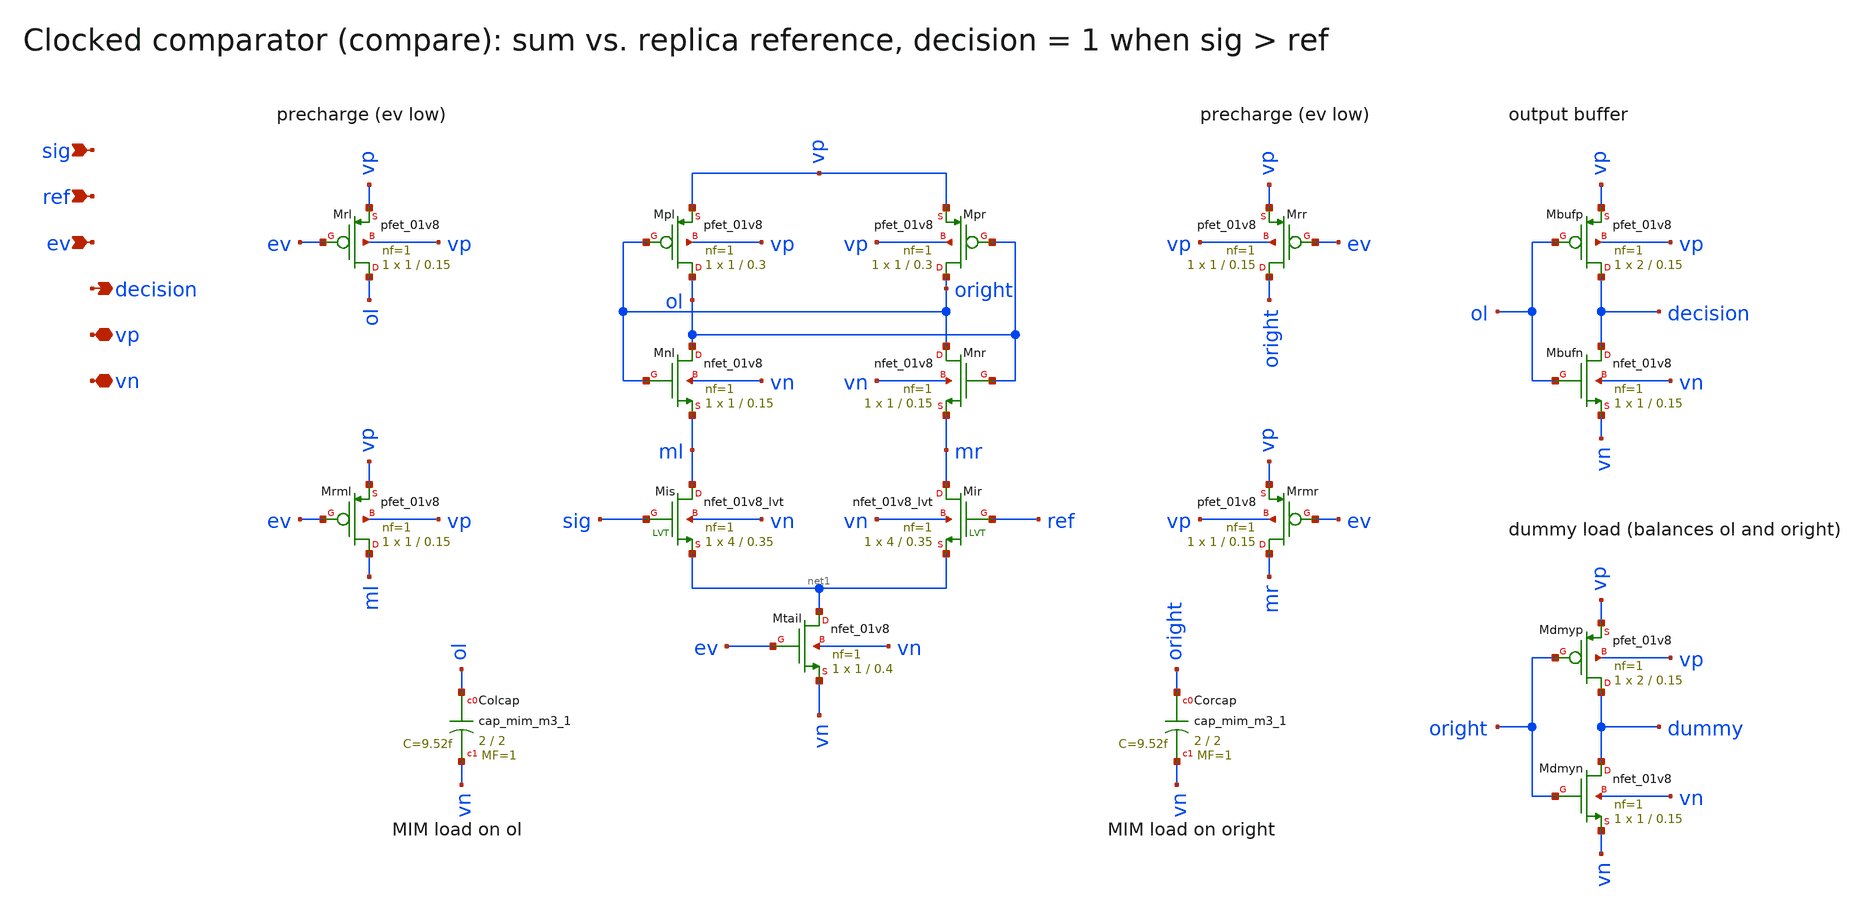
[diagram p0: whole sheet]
** sch_path: xschem/compare.sch
**.subckt compare sig ref ev decision vp vn
*.ipin sig
*.ipin ref
*.ipin ev
*.opin decision
*.iopin vp
*.iopin vn
XMpl ol oright vp vp sky130_fd_pr__pfet_01v8 L=0.3 W=1 nf=1 ad='int((nf+1)/2) * W/nf * 0.29' as='int((nf+2)/2) * W/nf * 0.29'
+ pd='2*int((nf+1)/2) * (W/nf + 0.29)' ps='2*int((nf+2)/2) * (W/nf + 0.29)' nrd=0 nrs=0 sa=0 sb=0 sd=0
+ mult=1 m=1
XMpr oright ol vp vp sky130_fd_pr__pfet_01v8 L=0.3 W=1 nf=1 ad='int((nf+1)/2) * W/nf * 0.29' as='int((nf+2)/2) * W/nf * 0.29'
+ pd='2*int((nf+1)/2) * (W/nf + 0.29)' ps='2*int((nf+2)/2) * (W/nf + 0.29)' nrd=0 nrs=0 sa=0 sb=0 sd=0
+ mult=1 m=1
XMnl ol oright ml vn sky130_fd_pr__nfet_01v8 L=0.15 W=1 nf=1 ad='int((nf+1)/2) * W/nf * 0.29' as='int((nf+2)/2) * W/nf * 0.29'
+ pd='2*int((nf+1)/2) * (W/nf + 0.29)' ps='2*int((nf+2)/2) * (W/nf + 0.29)' nrd=0 nrs=0 sa=0 sb=0 sd=0
+ mult=1 m=1
XMnr oright ol mr vn sky130_fd_pr__nfet_01v8 L=0.15 W=1 nf=1 ad='int((nf+1)/2) * W/nf * 0.29' as='int((nf+2)/2) * W/nf * 0.29'
+ pd='2*int((nf+1)/2) * (W/nf + 0.29)' ps='2*int((nf+2)/2) * (W/nf + 0.29)' nrd=0 nrs=0 sa=0 sb=0 sd=0
+ mult=1 m=1
XMis ml sig net1 vn sky130_fd_pr__nfet_01v8_lvt L=0.35 W=4 nf=1 ad='int((nf+1)/2) * W/nf * 0.29' as='int((nf+2)/2) * W/nf * 0.29'
+ pd='2*int((nf+1)/2) * (W/nf + 0.29)' ps='2*int((nf+2)/2) * (W/nf + 0.29)' nrd=0 nrs=0 sa=0 sb=0 sd=0
+ mult=1 m=1
XMir mr ref net1 vn sky130_fd_pr__nfet_01v8_lvt L=0.35 W=4 nf=1 ad='int((nf+1)/2) * W/nf * 0.29' as='int((nf+2)/2) * W/nf * 0.29'
+ pd='2*int((nf+1)/2) * (W/nf + 0.29)' ps='2*int((nf+2)/2) * (W/nf + 0.29)' nrd=0 nrs=0 sa=0 sb=0 sd=0
+ mult=1 m=1
XMtail net1 ev vn vn sky130_fd_pr__nfet_01v8 L=0.4 W=1 nf=1 ad='int((nf+1)/2) * W/nf * 0.29' as='int((nf+2)/2) * W/nf * 0.29'
+ pd='2*int((nf+1)/2) * (W/nf + 0.29)' ps='2*int((nf+2)/2) * (W/nf + 0.29)' nrd=0 nrs=0 sa=0 sb=0 sd=0
+ mult=1 m=1
XMrl ol ev vp vp sky130_fd_pr__pfet_01v8 L=0.15 W=1 nf=1 ad='int((nf+1)/2) * W/nf * 0.29' as='int((nf+2)/2) * W/nf * 0.29'
+ pd='2*int((nf+1)/2) * (W/nf + 0.29)' ps='2*int((nf+2)/2) * (W/nf + 0.29)' nrd=0 nrs=0 sa=0 sb=0 sd=0
+ mult=1 m=1
XMrml ml ev vp vp sky130_fd_pr__pfet_01v8 L=0.15 W=1 nf=1 ad='int((nf+1)/2) * W/nf * 0.29' as='int((nf+2)/2) * W/nf * 0.29'
+ pd='2*int((nf+1)/2) * (W/nf + 0.29)' ps='2*int((nf+2)/2) * (W/nf + 0.29)' nrd=0 nrs=0 sa=0 sb=0 sd=0
+ mult=1 m=1
XMrr oright ev vp vp sky130_fd_pr__pfet_01v8 L=0.15 W=1 nf=1 ad='int((nf+1)/2) * W/nf * 0.29' as='int((nf+2)/2) * W/nf * 0.29'
+ pd='2*int((nf+1)/2) * (W/nf + 0.29)' ps='2*int((nf+2)/2) * (W/nf + 0.29)' nrd=0 nrs=0 sa=0 sb=0 sd=0
+ mult=1 m=1
XMrmr mr ev vp vp sky130_fd_pr__pfet_01v8 L=0.15 W=1 nf=1 ad='int((nf+1)/2) * W/nf * 0.29' as='int((nf+2)/2) * W/nf * 0.29'
+ pd='2*int((nf+1)/2) * (W/nf + 0.29)' ps='2*int((nf+2)/2) * (W/nf + 0.29)' nrd=0 nrs=0 sa=0 sb=0 sd=0
+ mult=1 m=1
XColcap ol vn sky130_fd_pr__cap_mim_m3_1 W=2 L=2 MF=1 m=1
XCorcap oright vn sky130_fd_pr__cap_mim_m3_1 W=2 L=2 MF=1 m=1
XMbufp decision ol vp vp sky130_fd_pr__pfet_01v8 L=0.15 W=2 nf=1 ad='int((nf+1)/2) * W/nf * 0.29' as='int((nf+2)/2) * W/nf * 0.29'
+ pd='2*int((nf+1)/2) * (W/nf + 0.29)' ps='2*int((nf+2)/2) * (W/nf + 0.29)' nrd=0 nrs=0 sa=0 sb=0 sd=0
+ mult=1 m=1
XMbufn decision ol vn vn sky130_fd_pr__nfet_01v8 L=0.15 W=1 nf=1 ad='int((nf+1)/2) * W/nf * 0.29' as='int((nf+2)/2) * W/nf * 0.29'
+ pd='2*int((nf+1)/2) * (W/nf + 0.29)' ps='2*int((nf+2)/2) * (W/nf + 0.29)' nrd=0 nrs=0 sa=0 sb=0 sd=0
+ mult=1 m=1
XMdmyp dummy oright vp vp sky130_fd_pr__pfet_01v8 L=0.15 W=2 nf=1 ad='int((nf+1)/2) * W/nf * 0.29' as='int((nf+2)/2) * W/nf * 0.29'
+ pd='2*int((nf+1)/2) * (W/nf + 0.29)' ps='2*int((nf+2)/2) * (W/nf + 0.29)' nrd=0 nrs=0 sa=0 sb=0 sd=0
+ mult=1 m=1
XMdmyn dummy oright vn vn sky130_fd_pr__nfet_01v8 L=0.15 W=1 nf=1 ad='int((nf+1)/2) * W/nf * 0.29' as='int((nf+2)/2) * W/nf * 0.29'
+ pd='2*int((nf+1)/2) * (W/nf + 0.29)' ps='2*int((nf+2)/2) * (W/nf + 0.29)' nrd=0 nrs=0 sa=0 sb=0 sd=0
+ mult=1 m=1
**.ends
.end
